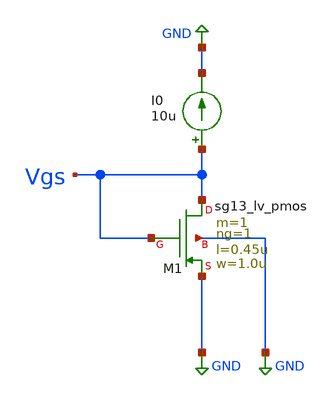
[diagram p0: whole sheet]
** sch_path: ihp-sg13g2/xschem_libs/sg13g2_tests_ase/mc_lv_pmos_cs_loop/schematic/mc_lv_pmos_cs_loop.sch
* Copyright 2023 IHP PDK Authors
**.subckt mc_lv_pmos_cs_loop
I0 Vgs GND 10u
XM1 Vgs Vgs GND GND sg13_lv_pmos w=1.0u l=0.45u ng=1 m=1 mm_ok=1
**.ends
.GLOBAL GND
.end
